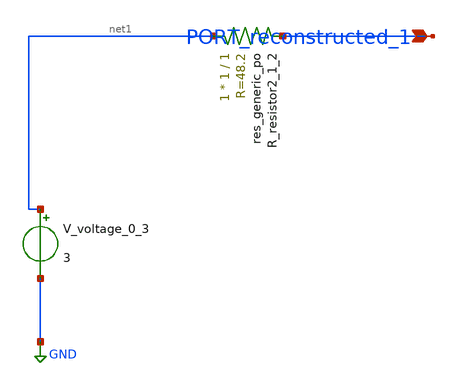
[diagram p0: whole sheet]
** sch_path: schematics/AMSNet/117.sch
**.subckt 117 PORT_reconstructed_1
*.ipin PORT_reconstructed_1
XR_resistor2_1_2 net1 PORT_reconstructed_1 sky130_fd_pr__res_generic_po W=1 L=1 m=1
V_voltage_0_3 net1 GND 3
**.ends
.GLOBAL GND
.end
